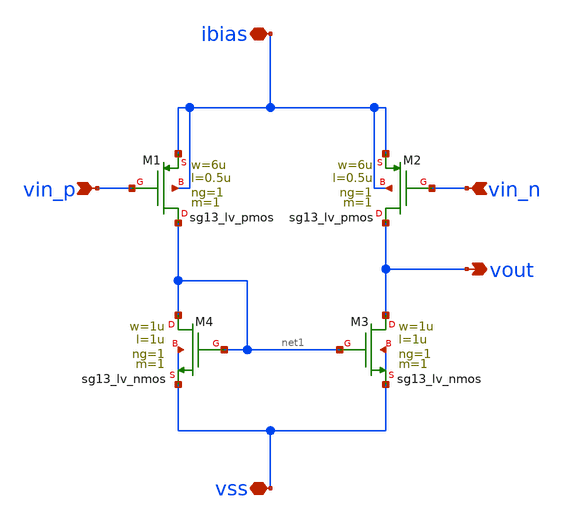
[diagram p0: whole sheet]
** sch_path: SSDOR_1.2V_v2/components/cgenerator/ota_cmp3.sch
**.subckt ota_cmp3 vss ibias vin_p vin_n vout
*.iopin vss
*.iopin ibias
*.ipin vin_p
*.ipin vin_n
*.opin vout
XM1 net1 vin_p ibias ibias sg13_lv_pmos w=6u l=0.5u ng=1 m=1 mm_ok=1
XM2 vout vin_n ibias ibias sg13_lv_pmos w=6u l=0.5u ng=1 m=1 mm_ok=1
XM3 vout net1 vss vss sg13_lv_nmos w=1u l=1u ng=1 m=1 mm_ok=1
XM4 net1 net1 vss vss sg13_lv_nmos w=1u l=1u ng=1 m=1 mm_ok=1
**.ends
.end
